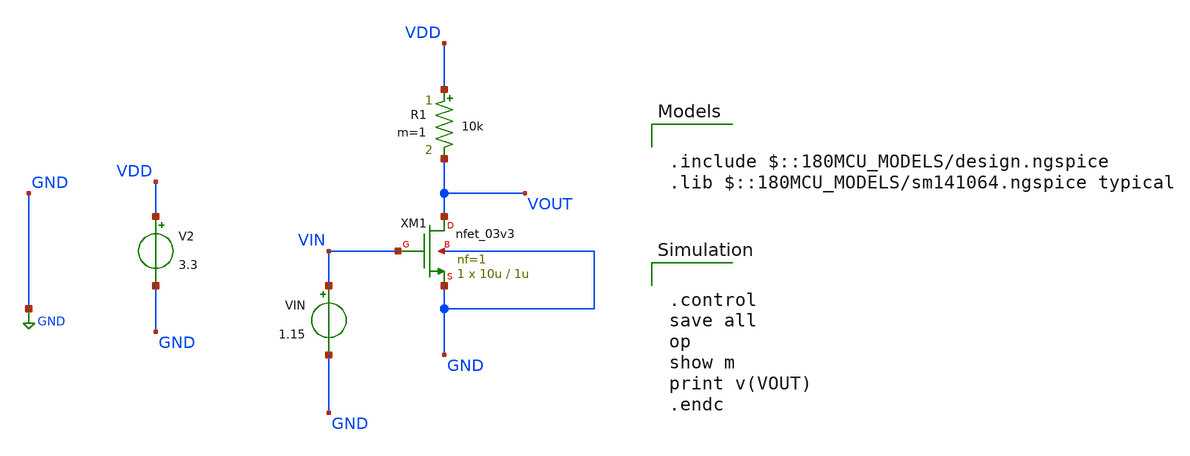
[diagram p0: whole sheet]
** sch_path: designs/sophiazhu/session_1/cs_res_load_dc_op.sch
**.subckt cs_res_load_dc_op
XM1 VOUT VIN GND GND nfet_03v3 L=1u W=10u nf=1 ad='int((nf+1)/2) * W/nf * 0.18u' as='int((nf+2)/2) * W/nf * 0.18u'
+ pd='2*int((nf+1)/2) * (W/nf + 0.18u)' ps='2*int((nf+2)/2) * (W/nf + 0.18u)' nrd='0.18u / W' nrs='0.18u / W'
+ sa=0 sb=0 sd=0 m=1
R1 VDD VOUT 10k m=1
V2 VDD GND 3.3
VIN VIN GND 1.15
**** begin user architecture code


.control
save all
op
show m
print v(VOUT)
.endc



.include $::180MCU_MODELS/design.ngspice
.lib $::180MCU_MODELS/sm141064.ngspice typical

**** end user architecture code
**.ends
.GLOBAL GND
.end
